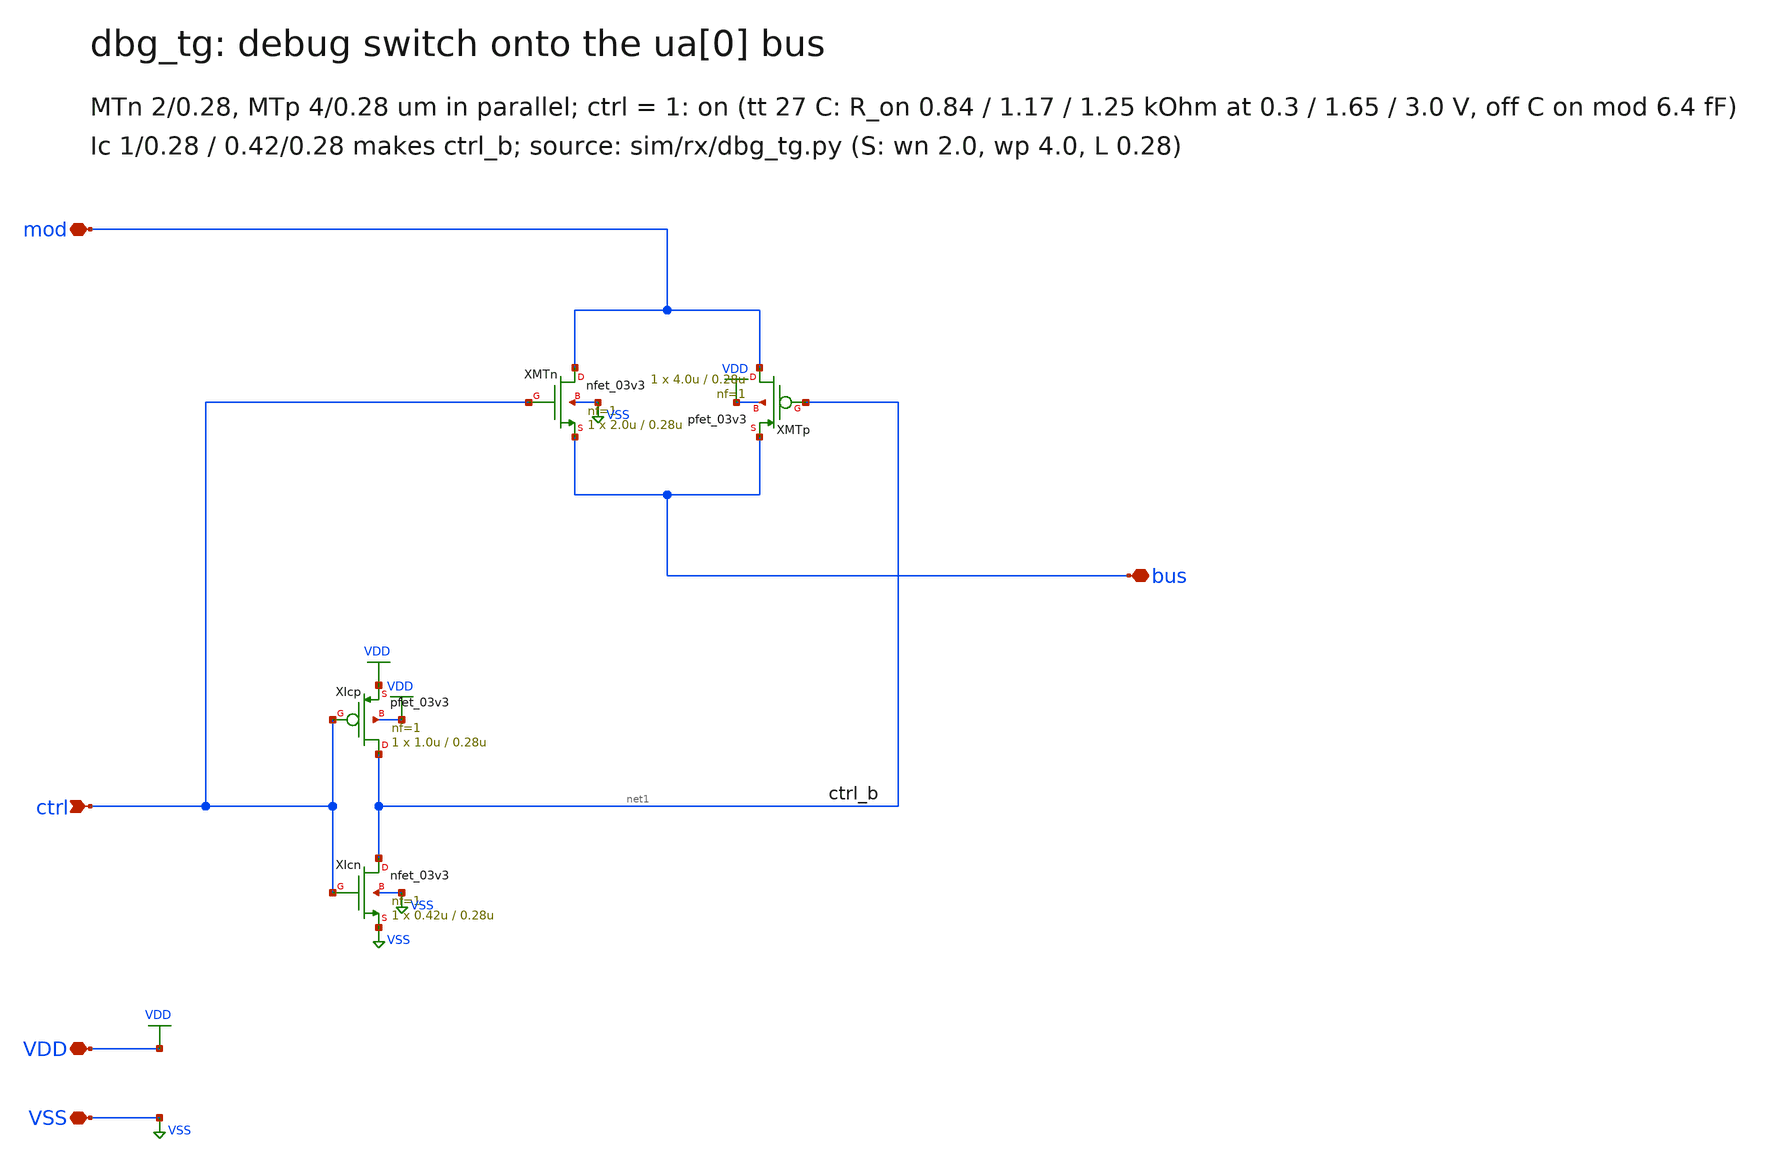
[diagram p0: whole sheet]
** sch_path: xschem/dbg_tg.sch
**.subckt dbg_tg VDD VSS ctrl mod bus
*.iopin VDD
*.iopin VSS
*.ipin ctrl
*.iopin mod
*.iopin bus
XMTn mod ctrl bus VSS nfet_03v3 L=0.28u W=2.0u nf=1 ad=1.0p as=1.0p pd=5.0u ps=5.0u nrd=0 nrs=0 sa=0
+ sb=0 sd=0 m=1
XMTp mod net1 bus VDD pfet_03v3 L=0.28u W=4.0u nf=1 ad=2.0p as=2.0p pd=9.0u ps=9.0u nrd=0 nrs=0 sa=0
+ sb=0 sd=0 m=1
XIcp net1 ctrl VDD VDD pfet_03v3 L=0.28u W=1.0u nf=1 ad=0.5p as=0.5p pd=3.0u ps=3.0u nrd=0 nrs=0
+ sa=0 sb=0 sd=0 m=1
XIcn net1 ctrl VSS VSS nfet_03v3 L=0.28u W=0.42u nf=1 ad=0.21p as=0.21p pd=1.8399999999999999u
+ ps=1.8399999999999999u nrd=0 nrs=0 sa=0 sb=0 sd=0 m=1
**.ends
.GLOBAL VSS
.GLOBAL VDD
.end
